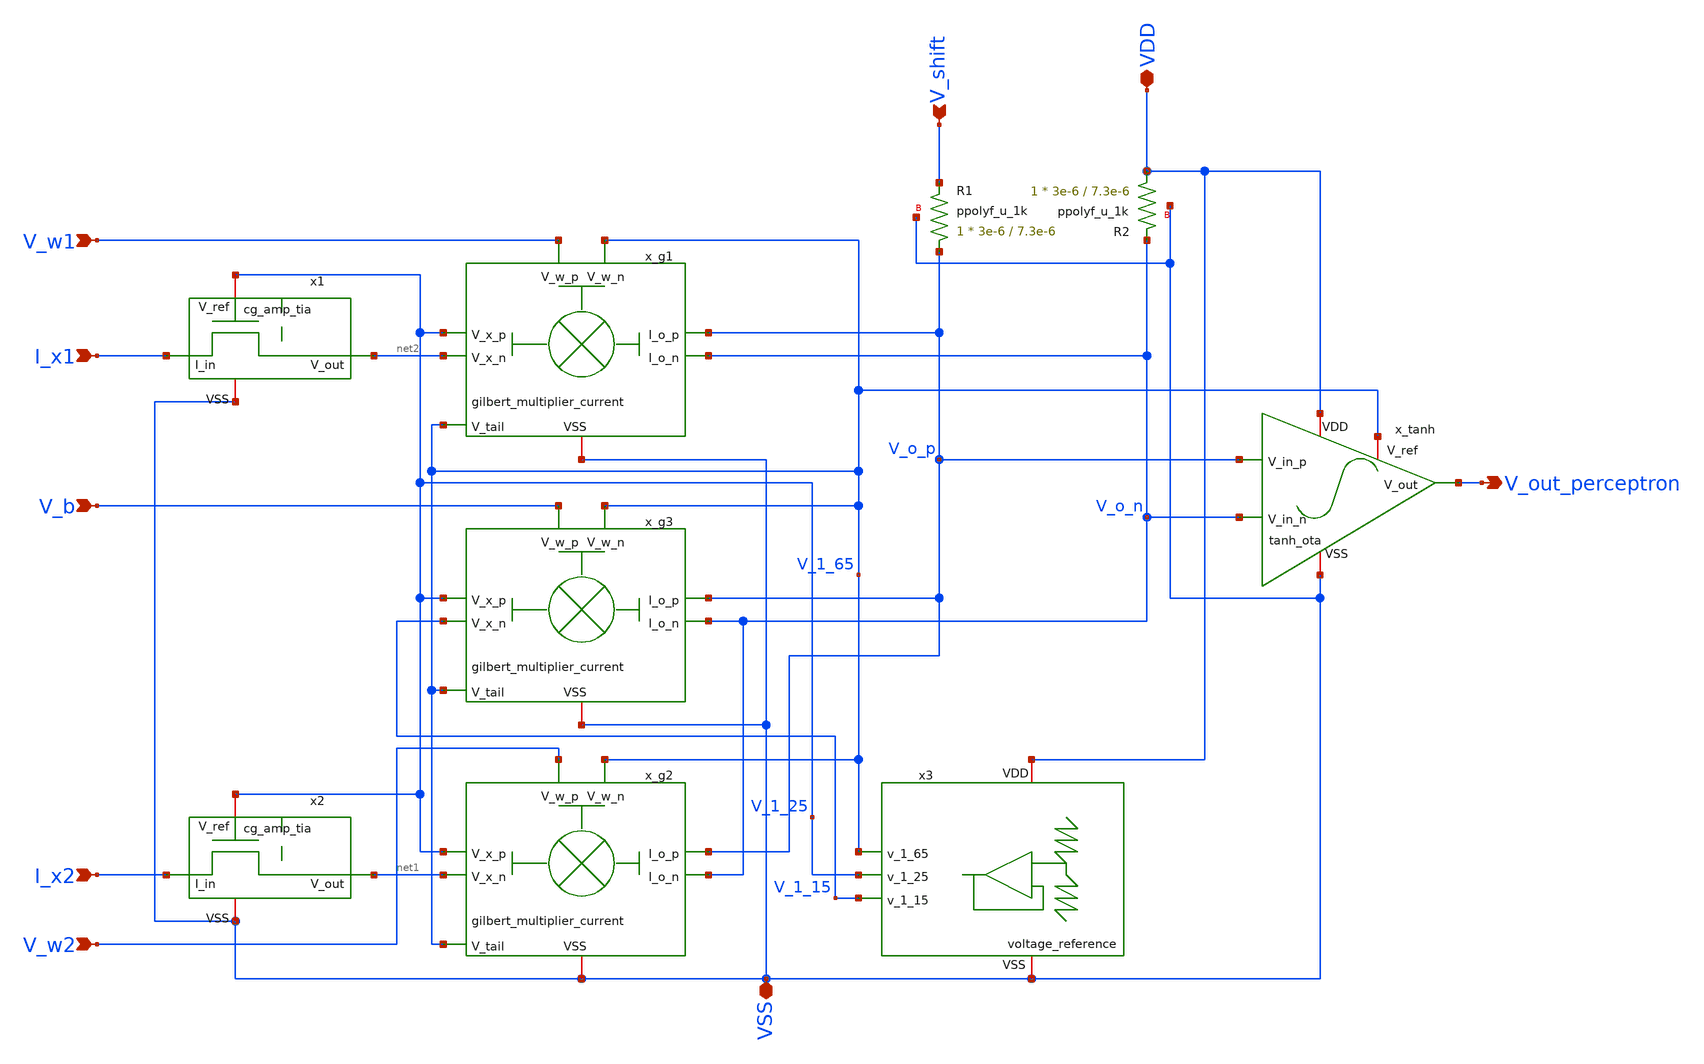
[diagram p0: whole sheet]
** sch_path: lvs/schematics/perceptron_core.sch
**.subckt perceptron_core VDD VSS I_x1 I_x2 V_w1 V_w2 V_b V_out_perceptron V_shift
*.iopin VDD
*.iopin VSS
*.ipin I_x1
*.ipin I_x2
*.ipin V_w1
*.ipin V_w2
*.ipin V_b
*.opin V_out_perceptron
*.ipin V_shift
x_g1 V_o_p V_o_n V_w1 V_1_65 V_1_25 net2 V_1_65 VSS gilbert_multiplier_current
x_g2 V_o_p V_o_n V_w2 V_1_65 V_1_25 net1 V_1_65 VSS gilbert_multiplier_current
x_g3 V_o_p V_o_n V_b V_1_65 V_1_25 V_1_15 V_1_65 VSS gilbert_multiplier_current
x_tanh VDD V_1_65 V_out_perceptron V_o_p V_o_n VSS tanh_ota
XR1 V_o_p V_shift VSS ppolyf_u_1k r_width=3e-6 r_length=7.3e-6 m=1
XR2 VDD V_o_n VSS ppolyf_u_1k r_width=3e-6 r_length=7.3e-6 m=1
x3 VDD V_1_65 V_1_25 V_1_15 VSS voltage_reference
x1 V_1_25 net2 I_x1 VSS cg_amp_tia
x2 V_1_25 net1 I_x2 VSS cg_amp_tia
**.ends
.end
